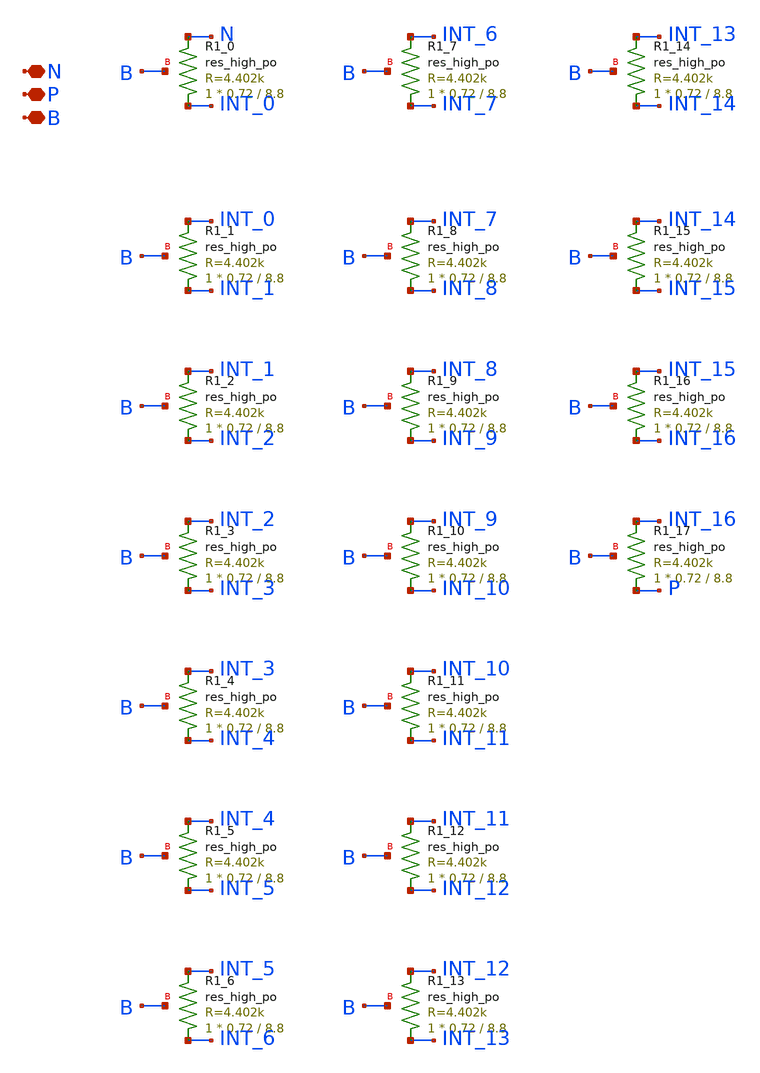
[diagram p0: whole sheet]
** sch_path: ip/sun_tr_sky130nm/design/SUN_TR_SKY130NM/SUNTR_RES200.sch
**.subckt SUNTR_RES200 N P B
*.iopin N
*.iopin P
*.iopin B
XR1_0 INT_0 N B sky130_fd_pr__res_high_po W=0.72 L=8.8 mult=1 m=1
XR1_1 INT_1 INT_0 B sky130_fd_pr__res_high_po W=0.72 L=8.8 mult=1 m=1
XR1_2 INT_2 INT_1 B sky130_fd_pr__res_high_po W=0.72 L=8.8 mult=1 m=1
XR1_3 INT_3 INT_2 B sky130_fd_pr__res_high_po W=0.72 L=8.8 mult=1 m=1
XR1_4 INT_4 INT_3 B sky130_fd_pr__res_high_po W=0.72 L=8.8 mult=1 m=1
XR1_5 INT_5 INT_4 B sky130_fd_pr__res_high_po W=0.72 L=8.8 mult=1 m=1
XR1_6 INT_6 INT_5 B sky130_fd_pr__res_high_po W=0.72 L=8.8 mult=1 m=1
XR1_7 INT_7 INT_6 B sky130_fd_pr__res_high_po W=0.72 L=8.8 mult=1 m=1
XR1_8 INT_8 INT_7 B sky130_fd_pr__res_high_po W=0.72 L=8.8 mult=1 m=1
XR1_9 INT_9 INT_8 B sky130_fd_pr__res_high_po W=0.72 L=8.8 mult=1 m=1
XR1_10 INT_10 INT_9 B sky130_fd_pr__res_high_po W=0.72 L=8.8 mult=1 m=1
XR1_11 INT_11 INT_10 B sky130_fd_pr__res_high_po W=0.72 L=8.8 mult=1 m=1
XR1_12 INT_12 INT_11 B sky130_fd_pr__res_high_po W=0.72 L=8.8 mult=1 m=1
XR1_13 INT_13 INT_12 B sky130_fd_pr__res_high_po W=0.72 L=8.8 mult=1 m=1
XR1_14 INT_14 INT_13 B sky130_fd_pr__res_high_po W=0.72 L=8.8 mult=1 m=1
XR1_15 INT_15 INT_14 B sky130_fd_pr__res_high_po W=0.72 L=8.8 mult=1 m=1
XR1_16 INT_16 INT_15 B sky130_fd_pr__res_high_po W=0.72 L=8.8 mult=1 m=1
XR1_17 P INT_16 B sky130_fd_pr__res_high_po W=0.72 L=8.8 mult=1 m=1
**.ends
.end
